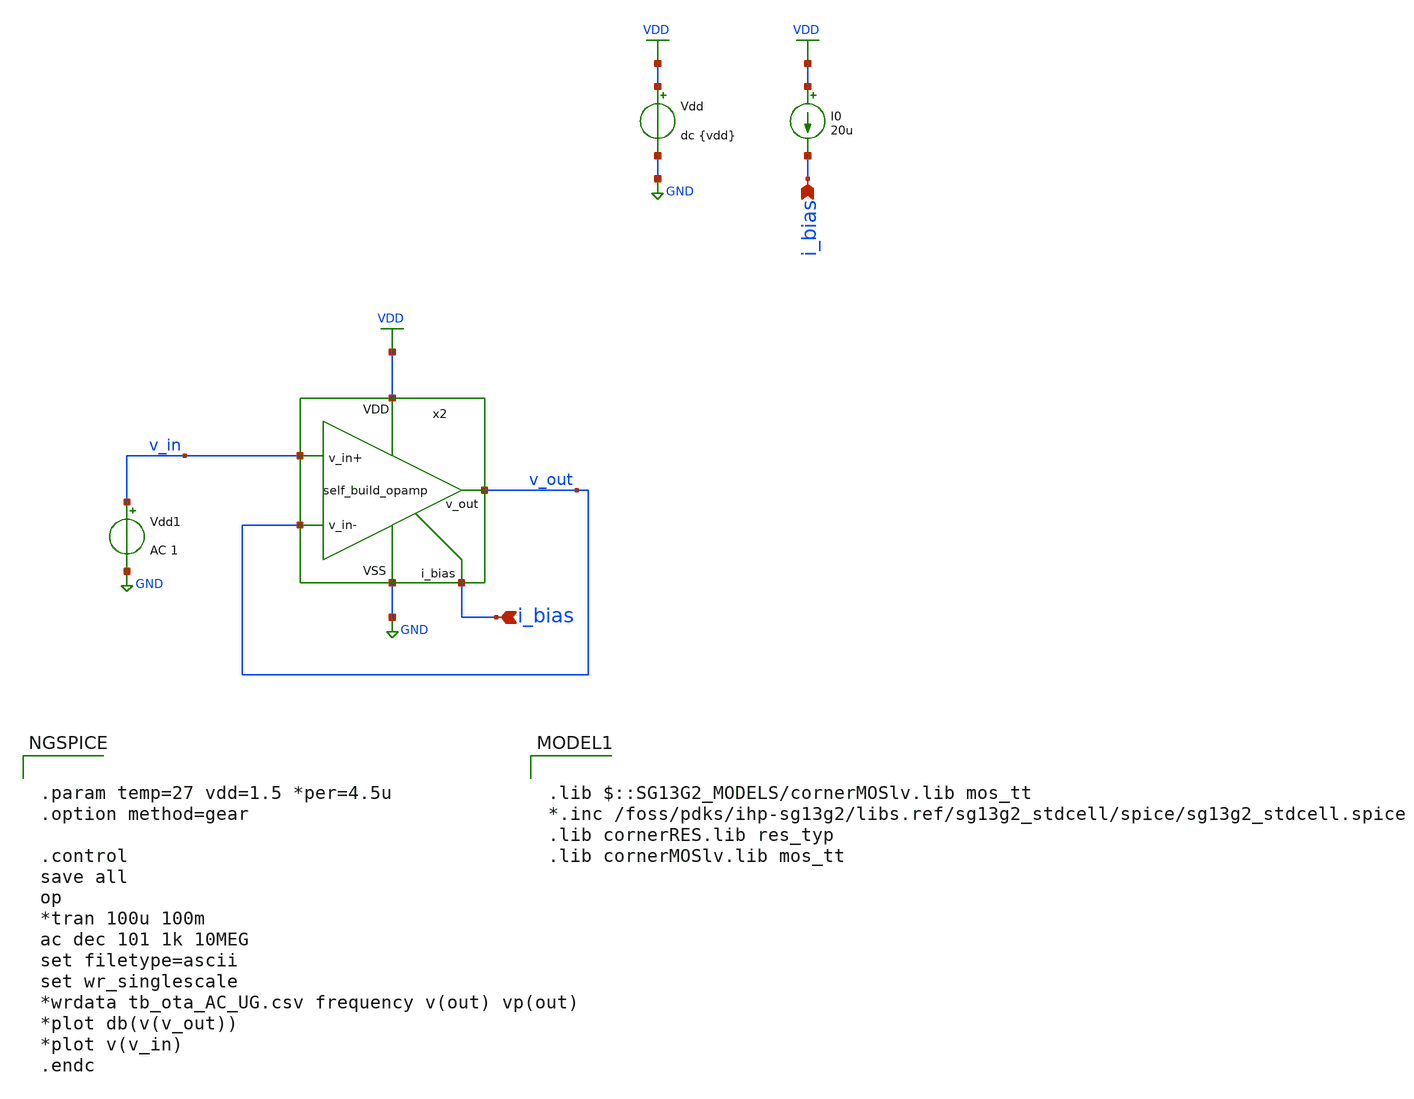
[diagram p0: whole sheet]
** sch_path: 3_Real_Cir/10_Real_Cir/tb_ota_ac.sch
**.subckt tb_ota_ac i_bias i_bias
*.ipin i_bias
*.ipin i_bias
Vdd VDD GND dc {vdd}
I0 VDD i_bias 20u
Vdd1 v_in GND AC 1
x2 v_out i_bias VDD GND v_in v_out self_build_opamp
**** begin user architecture code

.lib $::SG13G2_MODELS/cornerMOSlv.lib mos_tt
*.inc /foss/pdks/ihp-sg13g2/libs.ref/sg13g2_stdcell/spice/sg13g2_stdcell.spice
.lib cornerRES.lib res_typ
.lib cornerMOSlv.lib mos_tt



.param temp=27 vdd=1.5 *per=4.5u
.option method=gear

.control
save all
op
*tran 100u 100m
ac dec 101 1k 10MEG
set filetype=ascii
set wr_singlescale
*wrdata tb_ota_AC_UG.csv frequency v(out) vp(out)
*plot db(v(v_out))
*plot v(v_in)
.endc


**** end user architecture code
**.ends

* expanding   symbol:  3_Real_Cir/10_Real_Cir/self_build_opamp.sym # of pins=6
** sym_path: 3_Real_Cir/10_Real_Cir/self_build_opamp.sym
** sch_path: 3_Real_Cir/10_Real_Cir/self_build_opamp.sch
.subckt self_build_opamp v_out i_bias VDD VSS v_in+ v_in-
*.ipin v_in+
*.ipin v_in-
*.opin v_out
*.iopin VDD
*.iopin VSS
*.ipin i_bias
XM7 v_out v_imirror VDD VDD sg13_lv_pmos w=1.5u l=5u ng=1 m=1 mm_ok=1
XM1 v_imirror v_imirror VDD VDD sg13_lv_pmos w=1.5u l=5u ng=1 m=1 mm_ok=1
XM8 v_imirror v_in+ v_amp v_amp sg13_lv_nmos w=2u l=5u ng=1 m=1 mm_ok=1
XM3 v_out v_in- v_amp v_amp sg13_lv_nmos w=2u l=5u ng=1 m=1 mm_ok=1
XM2 v_amp i_bias VSS VSS sg13_lv_nmos w=0.5u l=5u ng=1 m=1 mm_ok=1
XM4 i_bias i_bias VSS VSS sg13_lv_nmos w=2.5u l=5u ng=1 m=1 mm_ok=1
x1 net1 net2 net3 net4 net5 net6 self_build_opamp
.ends

.GLOBAL GND
.GLOBAL VDD
.end
